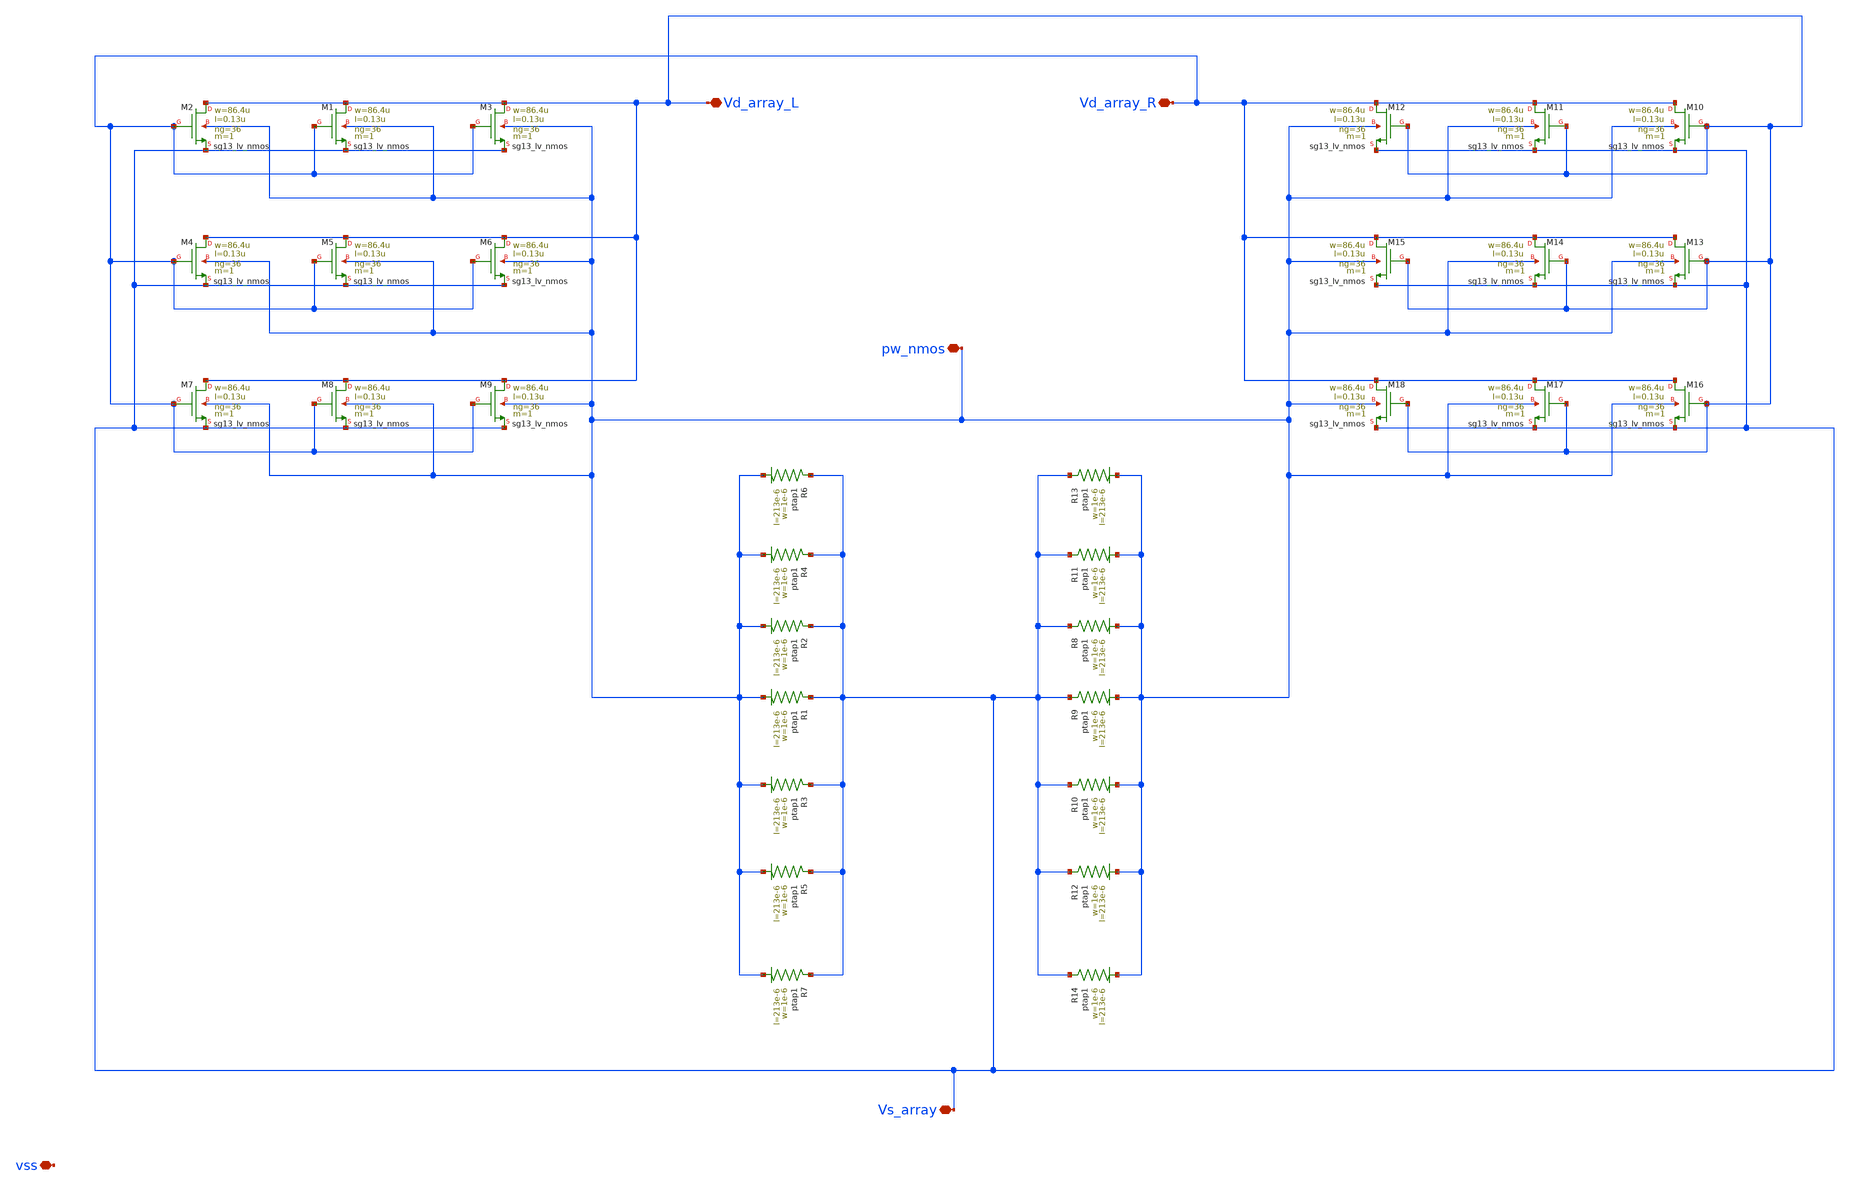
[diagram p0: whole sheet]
** sch_path: Layouts/PMOS/nmos_array_x2.sch
**.subckt nmos_array_x2 Vd_array_L Vs_array Vd_array_R pw_nmos vss
*.iopin Vd_array_L
*.iopin Vs_array
*.iopin Vd_array_R
*.iopin pw_nmos
*.iopin vss
XM2 Vd_array_L Vd_array_R Vs_array pw_nmos sg13_lv_nmos w=86.4u l=0.13u ng=36 m=1 mm_ok=1
XR2 Vs_array pw_nmos ptap1 R=1.529 w=1e-6 l=213e-6
XM1 Vd_array_L Vd_array_R Vs_array pw_nmos sg13_lv_nmos w=86.4u l=0.13u ng=36 m=1 mm_ok=1
XM3 Vd_array_L Vd_array_R Vs_array pw_nmos sg13_lv_nmos w=86.4u l=0.13u ng=36 m=1 mm_ok=1
XM4 Vd_array_L Vd_array_R Vs_array pw_nmos sg13_lv_nmos w=86.4u l=0.13u ng=36 m=1 mm_ok=1
XM5 Vd_array_L Vd_array_R Vs_array pw_nmos sg13_lv_nmos w=86.4u l=0.13u ng=36 m=1 mm_ok=1
XM6 Vd_array_L Vd_array_R Vs_array pw_nmos sg13_lv_nmos w=86.4u l=0.13u ng=36 m=1 mm_ok=1
XM7 Vd_array_L Vd_array_R Vs_array pw_nmos sg13_lv_nmos w=86.4u l=0.13u ng=36 m=1 mm_ok=1
XM8 Vd_array_L Vd_array_R Vs_array pw_nmos sg13_lv_nmos w=86.4u l=0.13u ng=36 m=1 mm_ok=1
XM9 Vd_array_L Vd_array_R Vs_array pw_nmos sg13_lv_nmos w=86.4u l=0.13u ng=36 m=1 mm_ok=1
XR1 Vs_array pw_nmos ptap1 R=1.529 w=1e-6 l=213e-6
XR3 Vs_array pw_nmos ptap1 R=1.529 w=1e-6 l=213e-6
XR4 Vs_array pw_nmos ptap1 R=1.529 w=1e-6 l=213e-6
XR5 Vs_array pw_nmos ptap1 R=1.529 w=1e-6 l=213e-6
XR6 Vs_array pw_nmos ptap1 R=1.529 w=1e-6 l=213e-6
XR7 Vs_array pw_nmos ptap1 R=1.529 w=1e-6 l=213e-6
XM10 Vd_array_R Vd_array_L Vs_array pw_nmos sg13_lv_nmos w=86.4u l=0.13u ng=36 m=1 mm_ok=1
XR8 Vs_array pw_nmos ptap1 R=1.529 w=1e-6 l=213e-6
XM11 Vd_array_R Vd_array_L Vs_array pw_nmos sg13_lv_nmos w=86.4u l=0.13u ng=36 m=1 mm_ok=1
XM12 Vd_array_R Vd_array_L Vs_array pw_nmos sg13_lv_nmos w=86.4u l=0.13u ng=36 m=1 mm_ok=1
XM13 Vd_array_R Vd_array_L Vs_array pw_nmos sg13_lv_nmos w=86.4u l=0.13u ng=36 m=1 mm_ok=1
XM14 Vd_array_R Vd_array_L Vs_array pw_nmos sg13_lv_nmos w=86.4u l=0.13u ng=36 m=1 mm_ok=1
XM15 Vd_array_R Vd_array_L Vs_array pw_nmos sg13_lv_nmos w=86.4u l=0.13u ng=36 m=1 mm_ok=1
XM16 Vd_array_R Vd_array_L Vs_array pw_nmos sg13_lv_nmos w=86.4u l=0.13u ng=36 m=1 mm_ok=1
XM17 Vd_array_R Vd_array_L Vs_array pw_nmos sg13_lv_nmos w=86.4u l=0.13u ng=36 m=1 mm_ok=1
XM18 Vd_array_R Vd_array_L Vs_array pw_nmos sg13_lv_nmos w=86.4u l=0.13u ng=36 m=1 mm_ok=1
XR9 Vs_array pw_nmos ptap1 R=1.529 w=1e-6 l=213e-6
XR10 Vs_array pw_nmos ptap1 R=1.529 w=1e-6 l=213e-6
XR11 Vs_array pw_nmos ptap1 R=1.529 w=1e-6 l=213e-6
XR12 Vs_array pw_nmos ptap1 R=1.529 w=1e-6 l=213e-6
XR13 Vs_array pw_nmos ptap1 R=1.529 w=1e-6 l=213e-6
XR14 Vs_array pw_nmos ptap1 R=1.529 w=1e-6 l=213e-6
**.ends
.end
